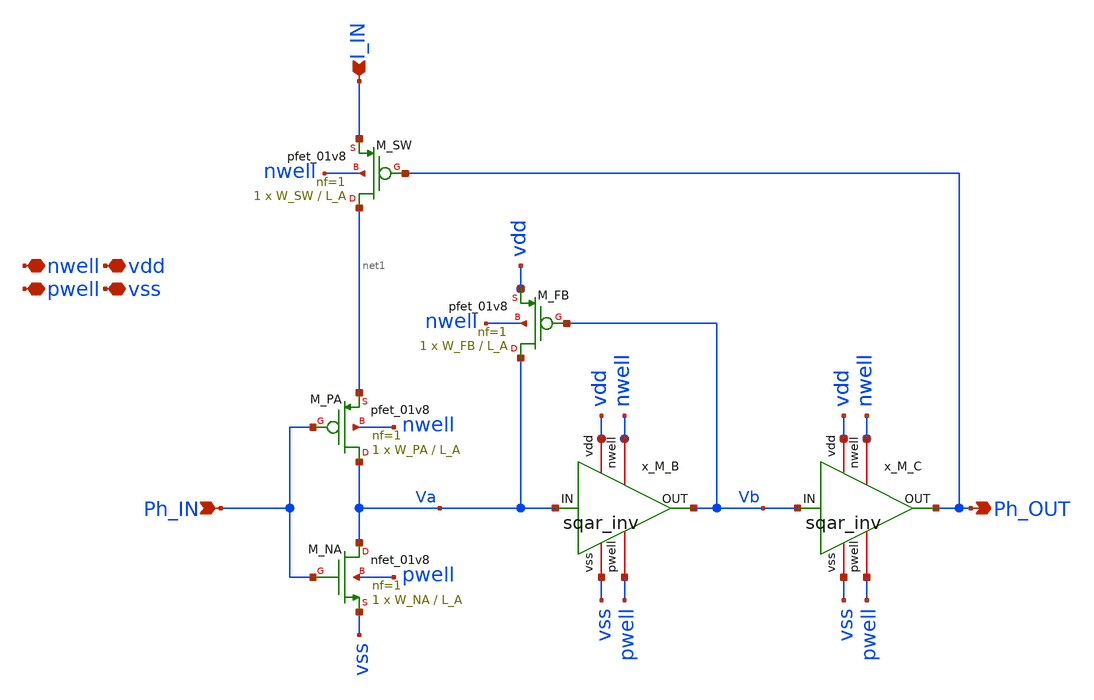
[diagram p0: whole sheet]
** sch_path: design/core/delay_cell/delay_cell.sch
**.subckt delay_cell vdd vss nwell pwell Ph_OUT I_IN Ph_IN
*.iopin vdd
*.iopin vss
*.iopin nwell
*.iopin pwell
*.opin Ph_OUT
*.ipin I_IN
*.ipin Ph_IN
XM_PA Va Ph_IN net1 nwell sky130_fd_pr__pfet_01v8 L=L_A W=W_PA nf=1 ad='int((nf+1)/2) * W/nf * 0.29'
+ as='int((nf+2)/2) * W/nf * 0.29' pd='2*int((nf+1)/2) * (W/nf + 0.29)' ps='2*int((nf+2)/2) * (W/nf + 0.29)'
+ nrd='0.29 / W' nrs='0.29 / W' sa=0 sb=0 sd=0 mult=1 m=1
XM_NA Va Ph_IN vss pwell sky130_fd_pr__nfet_01v8 L=L_A W=W_NA nf=1 ad='int((nf+1)/2) * W/nf * 0.29' as='int((nf+2)/2) * W/nf * 0.29'
+ pd='2*int((nf+1)/2) * (W/nf + 0.29)' ps='2*int((nf+2)/2) * (W/nf + 0.29)' nrd='0.29 / W' nrs='0.29 / W'
+ sa=0 sb=0 sd=0 mult=1 m=1
XM_SW net1 Ph_OUT I_IN nwell sky130_fd_pr__pfet_01v8 L=L_A W=W_SW nf=1 ad='int((nf+1)/2) * W/nf * 0.29'
+ as='int((nf+2)/2) * W/nf * 0.29' pd='2*int((nf+1)/2) * (W/nf + 0.29)' ps='2*int((nf+2)/2) * (W/nf + 0.29)'
+ nrd='0.29 / W' nrs='0.29 / W' sa=0 sb=0 sd=0 mult=1 m=1
XM_FB Va Vb vdd nwell sky130_fd_pr__pfet_01v8 L=L_A W=W_FB nf=1 ad='int((nf+1)/2) * W/nf * 0.29' as='int((nf+2)/2) * W/nf * 0.29'
+ pd='2*int((nf+1)/2) * (W/nf + 0.29)' ps='2*int((nf+2)/2) * (W/nf + 0.29)' nrd='0.29 / W' nrs='0.29 / W'
+ sa=0 sb=0 sd=0 mult=1 m=1
x_M_B vdd nwell Vb Va pwell vss sqar_inv W_CN=1 W_CP=1 L_SQ=1
x_M_C vdd nwell Ph_OUT Vb pwell vss sqar_inv W_CN=1 W_CP=1 L_SQ=1
**.ends

* expanding   symbol:  core/sqar_inv/sqar_inv.sym # of pins=6
** sym_path: design/core/sqar_inv/sqar_inv.sym
** sch_path: design/core/sqar_inv/sqar_inv.sch
.subckt sqar_inv vdd nwell OUT IN pwell vss  W_CN=1 W_CP=1 L_SQ=1
*.ipin IN
*.opin OUT
*.iopin nwell
*.iopin pwell
*.iopin vss
*.iopin vdd
XM1 OUT IN vss pwell sky130_fd_pr__nfet_01v8 L=L_SQ W=W_CN nf=1 ad='int((nf+1)/2) * W/nf * 0.29' as='int((nf+2)/2) * W/nf * 0.29'
+ pd='2*int((nf+1)/2) * (W/nf + 0.29)' ps='2*int((nf+2)/2) * (W/nf + 0.29)' nrd='0.29 / W' nrs='0.29 / W'
+ sa=0 sb=0 sd=0 mult=1 m=1
XM2 OUT IN vdd nwell sky130_fd_pr__pfet_01v8 L=L_SQ W=W_CP nf=1 ad='int((nf+1)/2) * W/nf * 0.29' as='int((nf+2)/2) * W/nf * 0.29'
+ pd='2*int((nf+1)/2) * (W/nf + 0.29)' ps='2*int((nf+2)/2) * (W/nf + 0.29)' nrd='0.29 / W' nrs='0.29 / W'
+ sa=0 sb=0 sd=0 mult=1 m=1
.ends

.end
